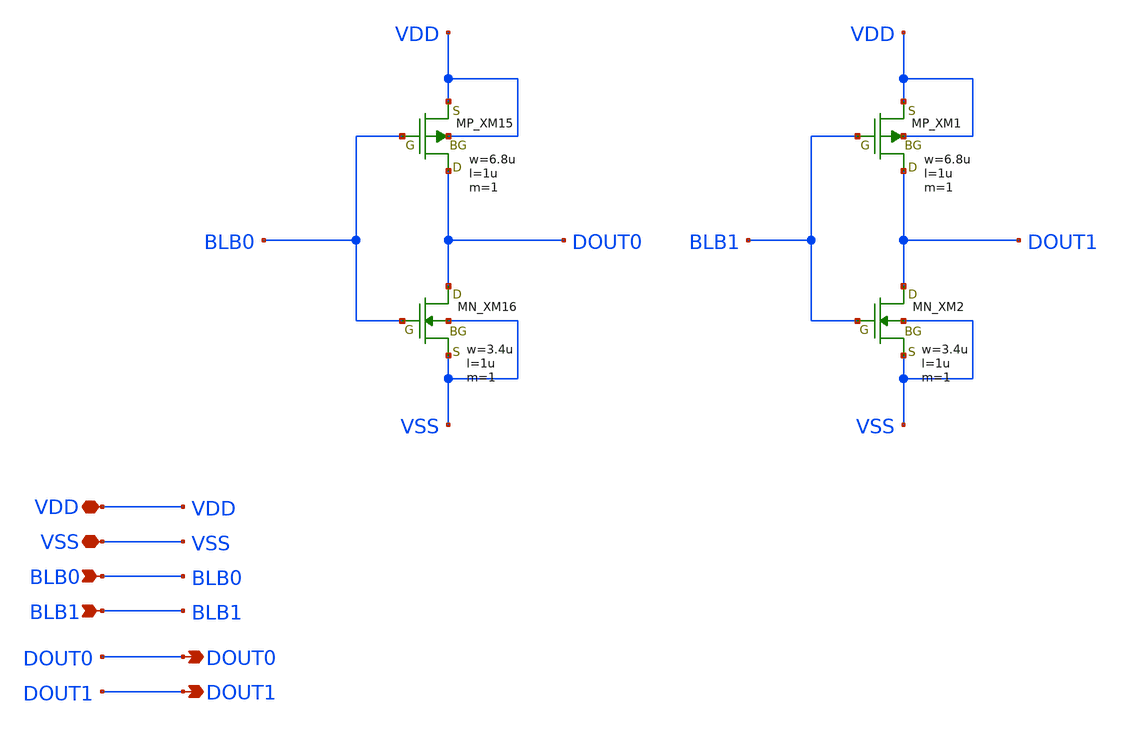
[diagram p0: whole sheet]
** sch_path: Deliverables/read_buffer.sch
**.subckt read_buffer VDD VSS BLB0 BLB1 DOUT0 DOUT1
*.iopin VDD
*.iopin VSS
*.ipin BLB0
*.ipin BLB1
*.opin DOUT0
*.opin DOUT1
XXM15 DOUT0 BLB0 VDD VDD PMOS w=6.8u l=1u nrd=0 nrs=0 m=1
XXM16 DOUT0 BLB0 VSS VSS NMOS w=3.4u l=1u nrd=0 nrs=0 m=1
XXM1 DOUT1 BLB1 VDD VDD PMOS w=6.8u l=1u nrd=0 nrs=0 m=1
XXM2 DOUT1 BLB1 VSS VSS NMOS w=3.4u l=1u nrd=0 nrs=0 m=1
**.ends
.end
